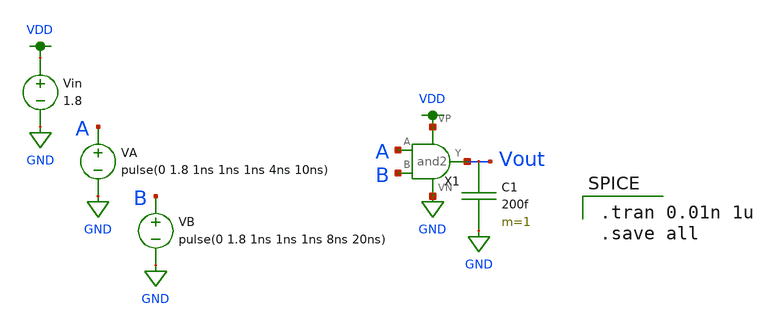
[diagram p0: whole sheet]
** sch_path: miniproject_01/xschem/and2_tran.sch
**.subckt and2_tran
Vin VDD GND 1.8
VA A GND pulse(0 1.8 1ns 1ns 1ns 4ns 10ns)
VB B GND pulse(0 1.8 1ns 1ns 1ns 8ns 20ns)
C1 Vout GND 200f m=1
X1 A Vout VDD GND B and2
**** begin user architecture code

.tran 0.01n 1u
.save all


.option wnflag=1
.lib ~/skywater/skywater-pdk/libraries/sky130_fd_pr_ngspice/latest/models/sky130.lib.spice tt

**** end user architecture code
**.ends

* expanding   symbol:  ENGR3426-MADVLSI/miniproject_01/xschem/and2.sym # of pins=5
** sym_path: miniproject_01/xschem/and2.sym
** sch_path: miniproject_01/xschem/and2.sch
.subckt and2 A Y VP VN B
*.ipin A
*.ipin B
*.iopin VP
*.iopin VN
*.opin Y
X1 A net1 VP VN B nand2
X2 net1 Y VP VN inverter
.ends


* expanding   symbol:  ENGR3426-MADVLSI/miniproject_01/xschem/nand2.sym # of pins=5
** sym_path: miniproject_01/xschem/nand2.sym
** sch_path: miniproject_01/xschem/nand2.sch
.subckt nand2 A Y VP VN B
*.opin Y
*.ipin B
*.ipin A
*.iopin VP
*.iopin VN
XM1 Y A net1 VN sky130_fd_pr__nfet_01v8 L=0.15 W=1 nf=1 ad='int((nf+1)/2) * W/nf * 0.29' as='int((nf+2)/2) * W/nf * 0.29'
+ pd='2*int((nf+1)/2) * (W/nf + 0.29)' ps='2*int((nf+2)/2) * (W/nf + 0.29)' nrd='0.29 / W' nrs='0.29 / W'
+ sa=0 sb=0 sd=0 mult=1 m=1
XM2 net1 B VN VN sky130_fd_pr__nfet_01v8 L=0.15 W=1 nf=1 ad='int((nf+1)/2) * W/nf * 0.29' as='int((nf+2)/2) * W/nf * 0.29'
+ pd='2*int((nf+1)/2) * (W/nf + 0.29)' ps='2*int((nf+2)/2) * (W/nf + 0.29)' nrd='0.29 / W' nrs='0.29 / W'
+ sa=0 sb=0 sd=0 mult=1 m=1
XM3 Y A VP VP sky130_fd_pr__pfet_01v8 L=0.15 W=1 nf=1 ad='int((nf+1)/2) * W/nf * 0.29' as='int((nf+2)/2) * W/nf * 0.29'
+ pd='2*int((nf+1)/2) * (W/nf + 0.29)' ps='2*int((nf+2)/2) * (W/nf + 0.29)' nrd='0.29 / W' nrs='0.29 / W'
+ sa=0 sb=0 sd=0 mult=1 m=1
XM4 VP B Y VP sky130_fd_pr__pfet_01v8 L=0.15 W=1 nf=1 ad='int((nf+1)/2) * W/nf * 0.29' as='int((nf+2)/2) * W/nf * 0.29'
+ pd='2*int((nf+1)/2) * (W/nf + 0.29)' ps='2*int((nf+2)/2) * (W/nf + 0.29)' nrd='0.29 / W' nrs='0.29 / W'
+ sa=0 sb=0 sd=0 mult=1 m=1
.ends


* expanding   symbol:  ENGR3426-MADVLSI/miniproject_01/xschem/inverter.sym # of pins=4
** sym_path: miniproject_01/xschem/inverter.sym
** sch_path: miniproject_01/xschem/inverter.sch
.subckt inverter A Y VP VN
*.ipin A
*.iopin VP
*.iopin VN
*.opin Y
XM1 Y A VN VN sky130_fd_pr__nfet_01v8 L=0.15 W=1 nf=1 ad='int((nf+1)/2) * W/nf * 0.29' as='int((nf+2)/2) * W/nf * 0.29'
+ pd='2*int((nf+1)/2) * (W/nf + 0.29)' ps='2*int((nf+2)/2) * (W/nf + 0.29)' nrd='0.29 / W' nrs='0.29 / W'
+ sa=0 sb=0 sd=0 mult=1 m=1
XM2 Y A VP VP sky130_fd_pr__pfet_01v8 L=0.15 W=1 nf=1 ad='int((nf+1)/2) * W/nf * 0.29' as='int((nf+2)/2) * W/nf * 0.29'
+ pd='2*int((nf+1)/2) * (W/nf + 0.29)' ps='2*int((nf+2)/2) * (W/nf + 0.29)' nrd='0.29 / W' nrs='0.29 / W'
+ sa=0 sb=0 sd=0 mult=1 m=1
.ends

.GLOBAL VDD
.GLOBAL GND
.end
